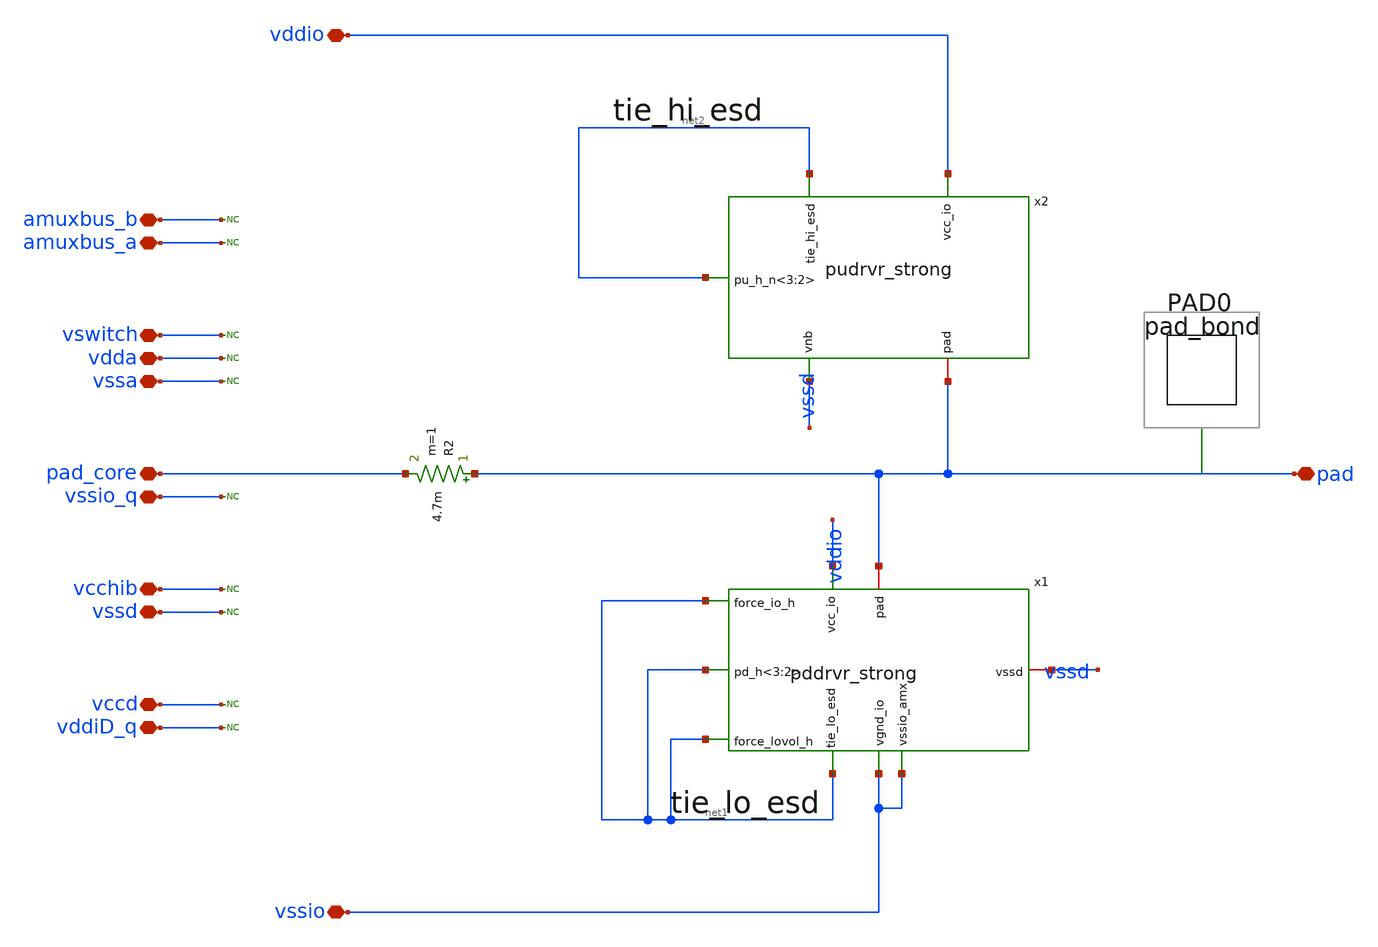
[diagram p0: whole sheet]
** sch_path: analogpad.sch
**.subckt analogpad vddio vssio pad amuxbus_b amuxbus_a vswitch vdda vssa pad_core vssio_q vcchib
*+ vssd vccd vddiD_q
*.iopin vddio
*.iopin vssio
*.iopin pad
*.iopin amuxbus_b
*.iopin amuxbus_a
*.iopin vswitch
*.iopin vdda
*.iopin vssa
*.iopin pad_core
*.iopin vssio_q
*.iopin vcchib
*.iopin vssd
*.iopin vccd
*.iopin vddiD_q
* noconn amuxbus_b
* noconn amuxbus_a
* noconn vswitch
* noconn vdda
* noconn vssa
* noconn vssio_q
* noconn vcchib
* noconn vssd
* noconn vccd
* noconn vddiD_q
R2 pad pad_core 4.7m m=1
x1 vddio vssd pad vssio net1 net1 net1 vssio net1 pddrvr_strong
x2 net2 vddio pad net2 vssd pudrvr_strong
**.ends
.end
